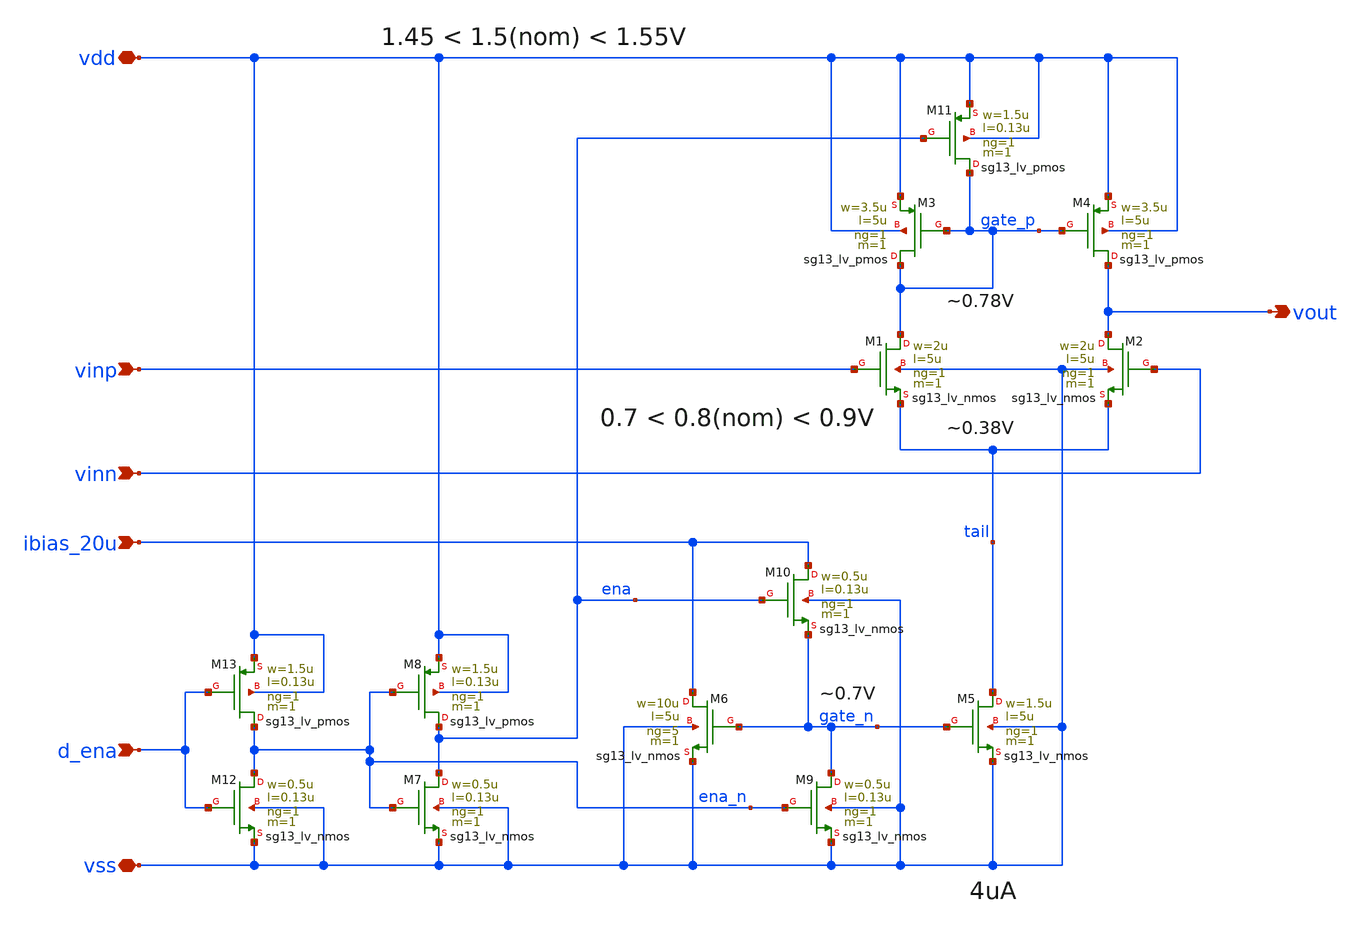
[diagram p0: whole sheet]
** sch_path: 004_Real_Circuits/001_version_basic_ota_pretl/ota-5t.sch
* (c) 2024-2025 Harald Pretl, Apache-2.0 license
**.subckt ota-5t ibias_20u vdd vss vinp vinn vout d_ena
*.ipin ibias_20u
*.iopin vdd
*.iopin vss
*.ipin vinp
*.ipin vinn
*.opin vout
*.ipin d_ena
XM5 tail gate_n vss vss sg13_lv_nmos w=1.5u l=5u ng=1 m=1 mm_ok=1
XM4 vout gate_p vdd vdd sg13_lv_pmos w=3.5u l=5u ng=1 m=1 mm_ok=1
XM1 gate_p vinp tail vss sg13_lv_nmos w=2u l=5u ng=1 m=1 mm_ok=1
XM2 vout vinn tail vss sg13_lv_nmos w=2u l=5u ng=1 m=1 mm_ok=1
XM3 gate_p gate_p vdd vdd sg13_lv_pmos w=3.5u l=5u ng=1 m=1 mm_ok=1
XM6 ibias_20u gate_n vss vss sg13_lv_nmos w=10u l=5u ng=5 m=1 mm_ok=1
XM9 gate_n ena_n vss vss sg13_lv_nmos w=0.5u l=0.13u ng=1 m=1 mm_ok=1
XM11 gate_p ena vdd vdd sg13_lv_pmos w=1.5u l=0.13u ng=1 m=1 mm_ok=1
XM7 ena ena_n vss vss sg13_lv_nmos w=0.5u l=0.13u ng=1 m=1 mm_ok=1
XM8 ena ena_n vdd vdd sg13_lv_pmos w=1.5u l=0.13u ng=1 m=1 mm_ok=1
XM10 ibias_20u ena gate_n vss sg13_lv_nmos w=0.5u l=0.13u ng=1 m=1 mm_ok=1
XM12 ena_n d_ena vss vss sg13_lv_nmos w=0.5u l=0.13u ng=1 m=1 mm_ok=1
XM13 ena_n d_ena vdd vdd sg13_lv_pmos w=1.5u l=0.13u ng=1 m=1 mm_ok=1
**.ends
.end
